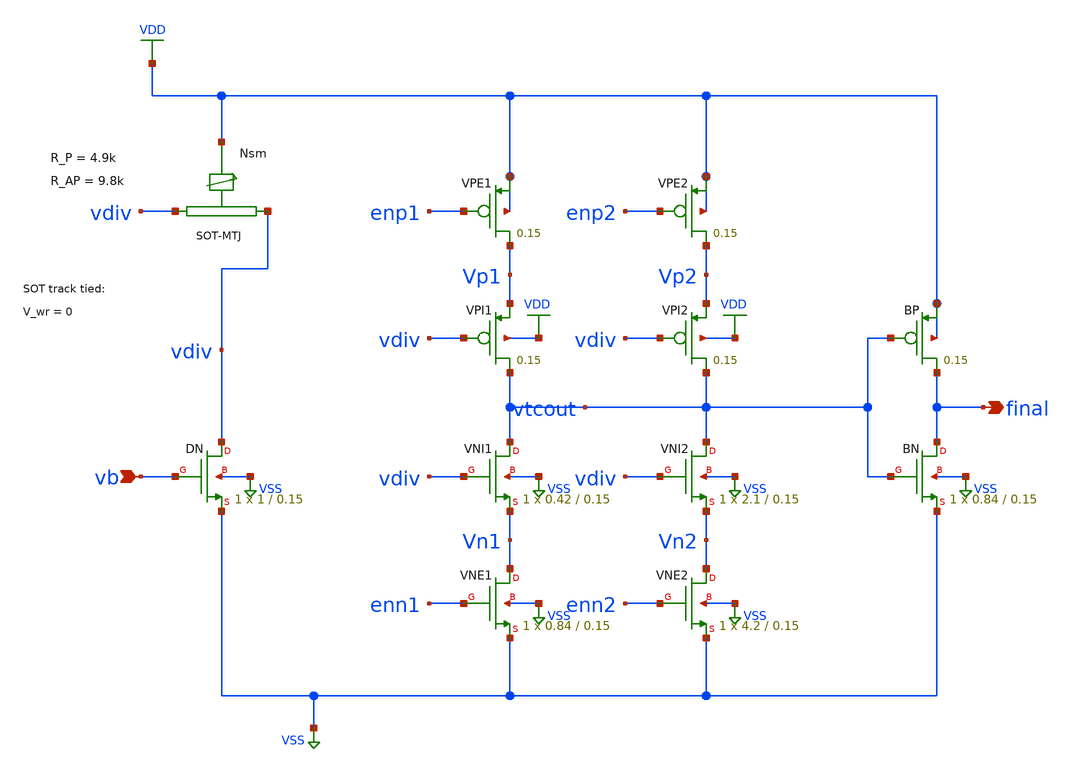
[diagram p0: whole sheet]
** sch_path: eda/hero/schematics/yoon_pbit_driver.sch
**.subckt yoon_pbit_driver vb final
*.ipin vb
*.opin final
XDN vdiv vb VSS VSS sky130_fd_pr__sky130_fd_pr__nfet_01v8 L=0.15 W=1 nrd='0.29 / W' nrs='0.29 / W' sa=0
+ sb=0 sd=0 mult=1 m=1
XVPE1 Vp1 enp1 VDD VDD sky130_fd_pr__sky130_fd_pr__pfet_01v8 L=0.15 W=0.84 nrd='0.29 / W' nrs='0.29 / W'
+ sa=0 sb=0 sd=0 mult=1 m=1
XVPI1 vtcout vdiv Vp1 VDD sky130_fd_pr__sky130_fd_pr__pfet_01v8 L=0.15 W=0.42 nrd='0.29 / W' nrs='0.29 / W'
+ sa=0 sb=0 sd=0 mult=1 m=1
XVNI1 vtcout vdiv Vn1 VSS sky130_fd_pr__sky130_fd_pr__nfet_01v8 L=0.15 W=0.42 nrd='0.29 / W' nrs='0.29 / W'
+ sa=0 sb=0 sd=0 mult=1 m=1
XVNE1 Vn1 enn1 VSS VSS sky130_fd_pr__sky130_fd_pr__nfet_01v8 L=0.15 W=0.84 nrd='0.29 / W' nrs='0.29 / W'
+ sa=0 sb=0 sd=0 mult=1 m=1
XVPE2 Vp2 enp2 VDD VDD sky130_fd_pr__sky130_fd_pr__pfet_01v8 L=0.15 W=26 nrd='0.29 / W' nrs='0.29 / W'
+ sa=0 sb=0 sd=0 mult=1 m=1
XVPI2 vtcout vdiv Vp2 VDD sky130_fd_pr__sky130_fd_pr__pfet_01v8 L=0.15 W=13 nrd='0.29 / W' nrs='0.29 / W'
+ sa=0 sb=0 sd=0 mult=1 m=1
XVNI2 vtcout vdiv Vn2 VSS sky130_fd_pr__sky130_fd_pr__nfet_01v8 L=0.15 W=2.1 nrd='0.29 / W' nrs='0.29 / W'
+ sa=0 sb=0 sd=0 mult=1 m=1
XVNE2 Vn2 enn2 VSS VSS sky130_fd_pr__sky130_fd_pr__nfet_01v8 L=0.15 W=4.2 nrd='0.29 / W' nrs='0.29 / W'
+ sa=0 sb=0 sd=0 mult=1 m=1
XBP final vtcout VDD VDD sky130_fd_pr__sky130_fd_pr__pfet_01v8 L=0.15 W=2 nrd='0.29 / W' nrs='0.29 / W'
+ sa=0 sb=0 sd=0 mult=1 m=1
XBN final vtcout VSS VSS sky130_fd_pr__sky130_fd_pr__nfet_01v8 L=0.15 W=0.84 nrd='0.29 / W' nrs='0.29 / W'
+ sa=0 sb=0 sd=0 mult=1 m=1
**.ends
.GLOBAL VSS
.GLOBAL VDD
.end
